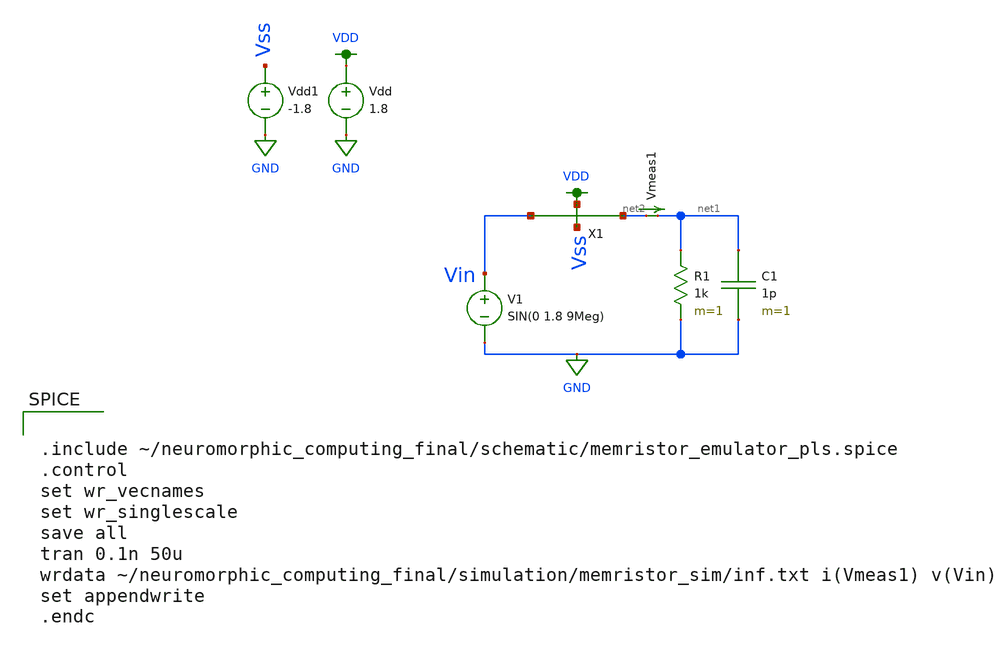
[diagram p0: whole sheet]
** sch_path: schematic/infinite_pls.sch
**.subckt infinite_pls
V1 Vin GND SIN(0 1.8 9Meg)
R1 net1 GND 1k m=1
C1 net1 GND 1p m=1
Vdd VDD GND 1.8
Vmeas1 net2 net1 0
.save i(vmeas1)
Vdd1 Vss GND -1.8
X1 VDD Vss net2 Vin memristor_emulator_pls
**** begin user architecture code


.include ~/neuromorphic_computing_final/schematic/memristor_emulator_pls.spice
.control
set wr_vecnames
set wr_singlescale
save all
tran 0.1n 50u
wrdata ~/neuromorphic_computing_final/simulation/memristor_sim/inf.txt i(Vmeas1) v(Vin)
set appendwrite
.endc



.option wnflag=1
.param MC_SWITCH=0.0
.lib ~/skywater/skywater-pdk/libraries/sky130_fd_pr_ngspice/latest/models/sky130.lib.spice tt

**** end user architecture code
**.ends
.GLOBAL VDD
.GLOBAL GND
.end
